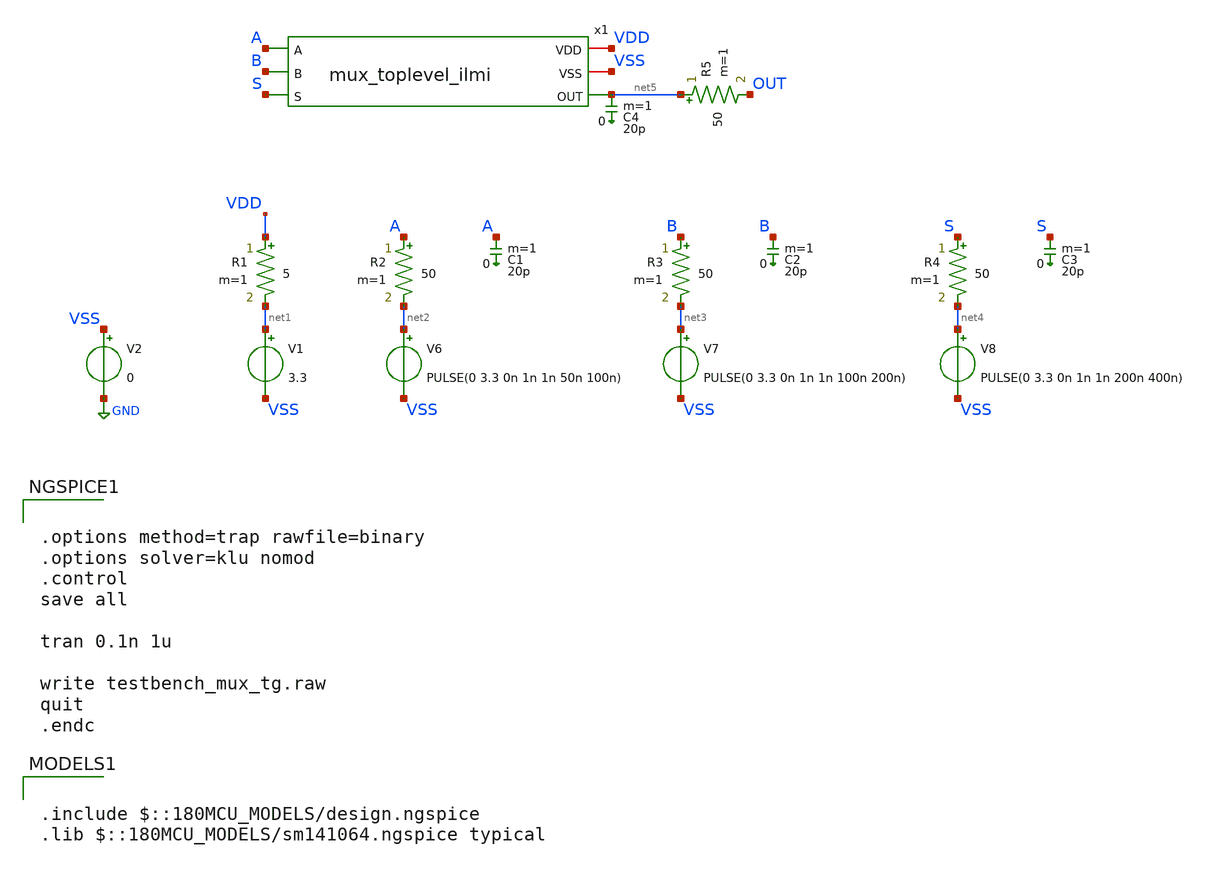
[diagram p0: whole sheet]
** sch_path: designs/libs/tb_mux/testbench_mux_tg_ilmi.sch
**.subckt testbench_mux_tg_ilmi
V6 net2 VSS PULSE(0 3.3 0n 1n 1n 50n 100n)
V7 net3 VSS PULSE(0 3.3 0n 1n 1n 100n 200n)
V8 net4 VSS PULSE(0 3.3 0n 1n 1n 200n 400n)
x1 A B VDD S VSS net5 mux_toplevel_ilmi
V1 net1 VSS 3.3
V2 VSS GND 0
R1 VDD net1 5 m=1
R2 A net2 50 m=1
R3 B net3 50 m=1
R4 S net4 50 m=1
C1 A 0 20p m=1
C2 B 0 20p m=1
C3 S 0 20p m=1
R5 net5 OUT 50 m=1
C4 net5 0 20p m=1
**** begin user architecture code

.include $::180MCU_MODELS/design.ngspice
.lib $::180MCU_MODELS/sm141064.ngspice typical



.options method=trap rawfile=binary
.options solver=klu nomod
.control
save all

tran 0.1n 1u

write testbench_mux_tg.raw
quit
.endc


**** end user architecture code
**.ends
.GLOBAL GND
.end
